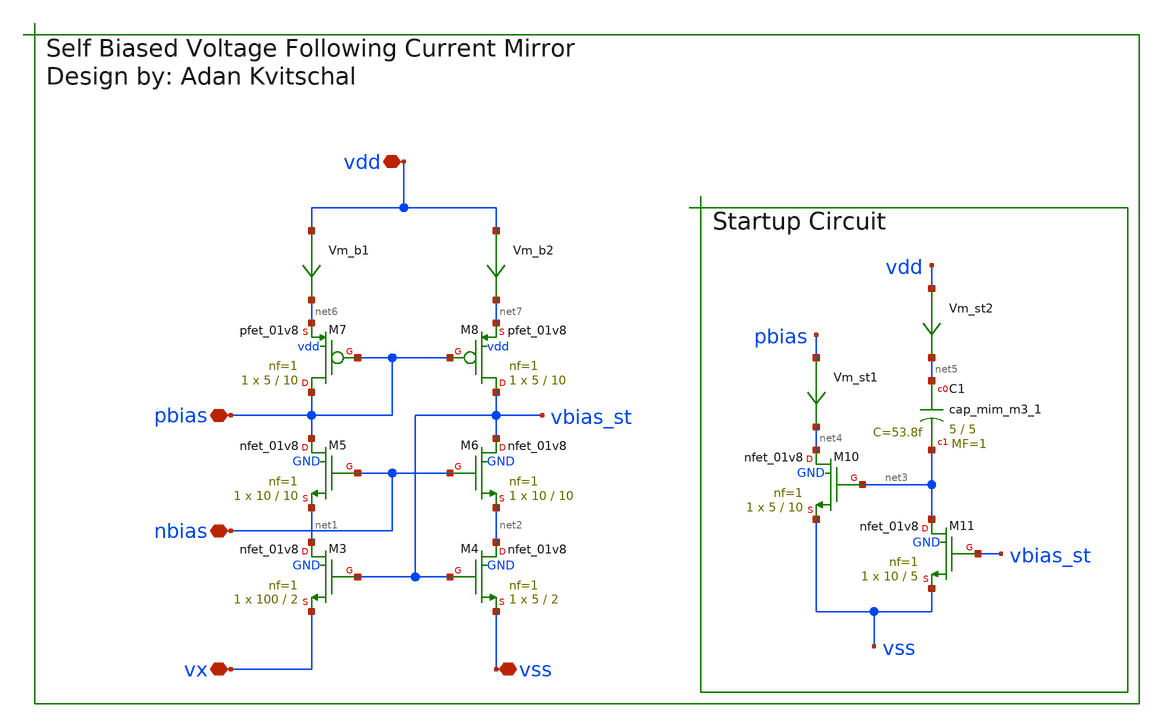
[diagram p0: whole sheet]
** sch_path: xschem/sbvfcm.sch
**.subckt sbvfcm vss vdd vx pbias nbias
*.iopin vss
*.iopin vdd
*.iopin vx
*.iopin pbias
*.iopin nbias
XM3 net1 vbias_st vx GND sky130_fd_pr__nfet_01v8 L=2 W=100 nf=1 ad='int((nf+1)/2) * W/nf * 0.29' as='int((nf+2)/2) * W/nf * 0.29'
+ pd='2*int((nf+1)/2) * (W/nf + 0.29)' ps='2*int((nf+2)/2) * (W/nf + 0.29)' nrd='0.29 / W' nrs='0.29 / W'
+ sa=0 sb=0 sd=0 mult=1 m=1
XM4 net2 vbias_st vss GND sky130_fd_pr__nfet_01v8 L=2 W=5 nf=1 ad='int((nf+1)/2) * W/nf * 0.29' as='int((nf+2)/2) * W/nf * 0.29'
+ pd='2*int((nf+1)/2) * (W/nf + 0.29)' ps='2*int((nf+2)/2) * (W/nf + 0.29)' nrd='0.29 / W' nrs='0.29 / W'
+ sa=0 sb=0 sd=0 mult=1 m=1
XM5 pbias nbias net1 GND sky130_fd_pr__nfet_01v8 L=10 W=10 nf=1 ad='int((nf+1)/2) * W/nf * 0.29' as='int((nf+2)/2) * W/nf * 0.29'
+ pd='2*int((nf+1)/2) * (W/nf + 0.29)' ps='2*int((nf+2)/2) * (W/nf + 0.29)' nrd='0.29 / W' nrs='0.29 / W'
+ sa=0 sb=0 sd=0 mult=1 m=1
XM6 vbias_st nbias net2 GND sky130_fd_pr__nfet_01v8 L=10 W=10 nf=1 ad='int((nf+1)/2) * W/nf * 0.29' as='int((nf+2)/2) * W/nf * 0.29'
+ pd='2*int((nf+1)/2) * (W/nf + 0.29)' ps='2*int((nf+2)/2) * (W/nf + 0.29)' nrd='0.29 / W' nrs='0.29 / W'
+ sa=0 sb=0 sd=0 mult=1 m=1
XM7 pbias pbias net6 vdd sky130_fd_pr__pfet_01v8 L=10 W=5 nf=1 ad='int((nf+1)/2) * W/nf * 0.29' as='int((nf+2)/2) * W/nf * 0.29'
+ pd='2*int((nf+1)/2) * (W/nf + 0.29)' ps='2*int((nf+2)/2) * (W/nf + 0.29)' nrd='0.29 / W' nrs='0.29 / W'
+ sa=0 sb=0 sd=0 mult=1 m=1
XM8 vbias_st pbias net7 vdd sky130_fd_pr__pfet_01v8 L=10 W=5 nf=1 ad='int((nf+1)/2) * W/nf * 0.29' as='int((nf+2)/2) * W/nf * 0.29'
+ pd='2*int((nf+1)/2) * (W/nf + 0.29)' ps='2*int((nf+2)/2) * (W/nf + 0.29)' nrd='0.29 / W' nrs='0.29 / W'
+ sa=0 sb=0 sd=0 mult=1 m=1
XM10 net4 net3 vss GND sky130_fd_pr__nfet_01v8 L=10 W=5 nf=1 ad='int((nf+1)/2) * W/nf * 0.29' as='int((nf+2)/2) * W/nf * 0.29'
+ pd='2*int((nf+1)/2) * (W/nf + 0.29)' ps='2*int((nf+2)/2) * (W/nf + 0.29)' nrd='0.29 / W' nrs='0.29 / W'
+ sa=0 sb=0 sd=0 mult=1 m=1
XM11 net3 vbias_st vss GND sky130_fd_pr__nfet_01v8 L=5 W=10 nf=1 ad='int((nf+1)/2) * W/nf * 0.29' as='int((nf+2)/2) * W/nf * 0.29'
+ pd='2*int((nf+1)/2) * (W/nf + 0.29)' ps='2*int((nf+2)/2) * (W/nf + 0.29)' nrd='0.29 / W' nrs='0.29 / W'
+ sa=0 sb=0 sd=0 mult=1 m=1
XC1 net5 net3 sky130_fd_pr__cap_mim_m3_1 W=5 L=5 MF=1 m=1
Vm_st1 pbias net4 0
.save i(vm_st1)
Vm_st2 vdd net5 0
.save i(vm_st2)
Vm_b1 vdd net6 0
.save i(vm_b1)
Vm_b2 vdd net7 0
.save i(vm_b2)
**.ends
.end
